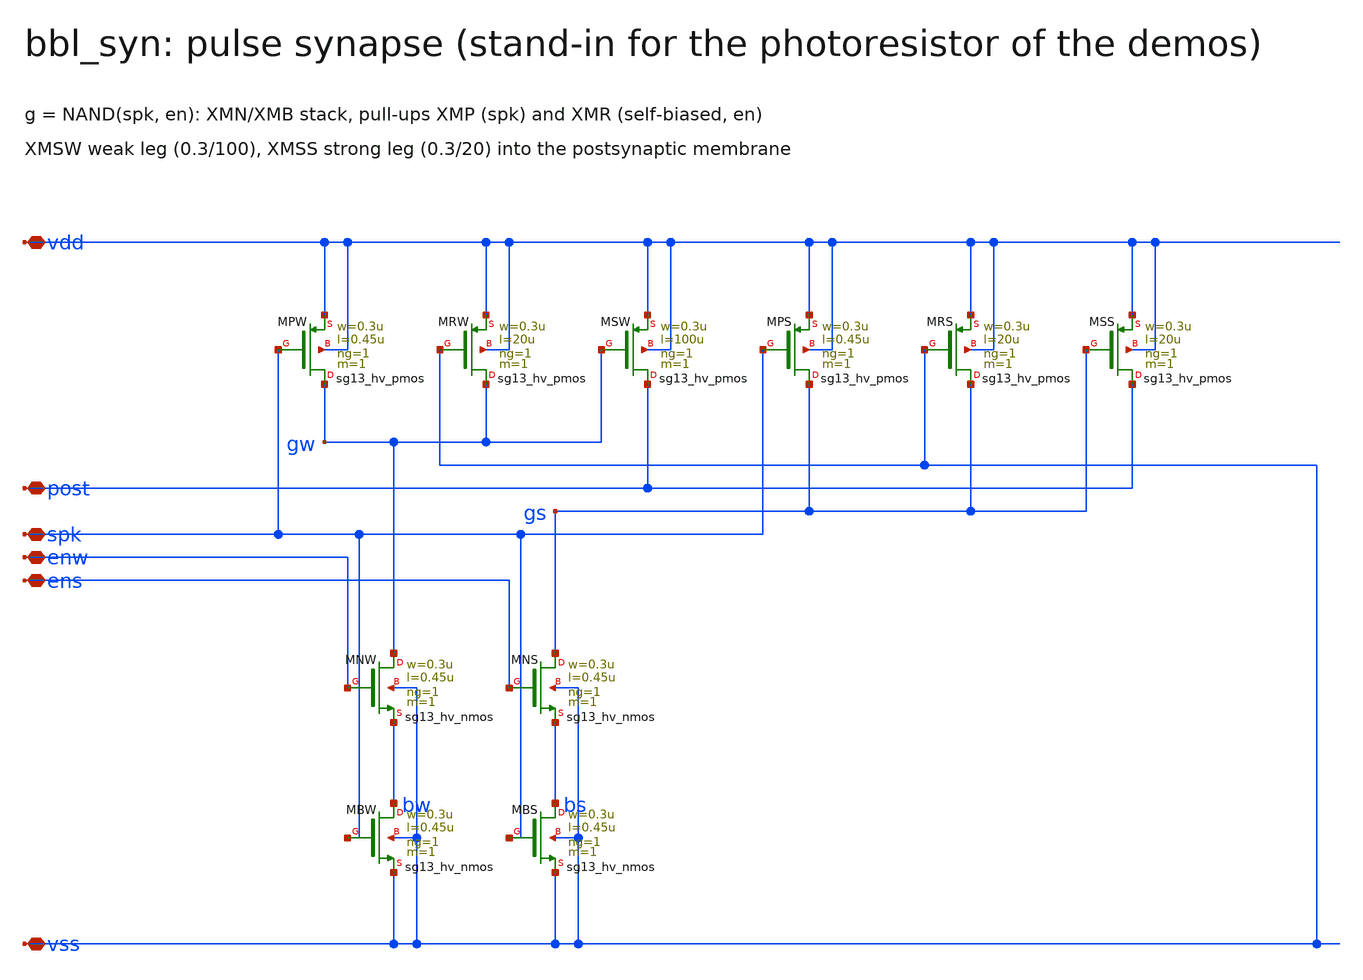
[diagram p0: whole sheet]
** sch_path: schematic/xschem/bbl_syn.sch
**.subckt bbl_syn vdd vss spk post enw ens
*.iopin vdd
*.iopin vss
*.iopin spk
*.iopin post
*.iopin enw
*.iopin ens
XMPW gw spk vdd vdd sg13_hv_pmos w=0.3u l=0.45u ng=1 m=1 mm_ok=1
XMRW gw vss vdd vdd sg13_hv_pmos w=0.3u l=20u ng=1 m=1 mm_ok=1
XMSW post gw vdd vdd sg13_hv_pmos w=0.3u l=100u ng=1 m=1 mm_ok=1
XMPS gs spk vdd vdd sg13_hv_pmos w=0.3u l=0.45u ng=1 m=1 mm_ok=1
XMRS gs vss vdd vdd sg13_hv_pmos w=0.3u l=20u ng=1 m=1 mm_ok=1
XMSS post gs vdd vdd sg13_hv_pmos w=0.3u l=20u ng=1 m=1 mm_ok=1
XMNW gw enw bw vss sg13_hv_nmos w=0.3u l=0.45u ng=1 m=1 mm_ok=1
XMNS gs ens bs vss sg13_hv_nmos w=0.3u l=0.45u ng=1 m=1 mm_ok=1
XMBW bw spk vss vss sg13_hv_nmos w=0.3u l=0.45u ng=1 m=1 mm_ok=1
XMBS bs spk vss vss sg13_hv_nmos w=0.3u l=0.45u ng=1 m=1 mm_ok=1
**.ends
.end
